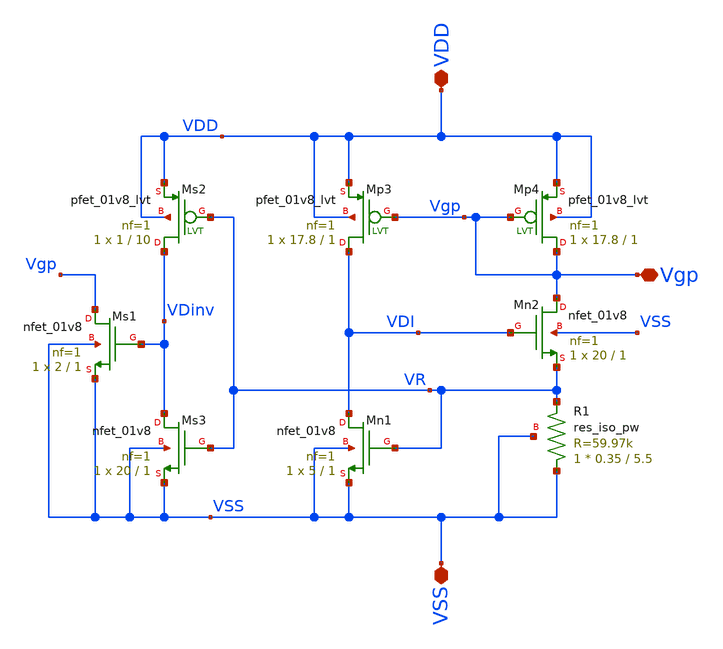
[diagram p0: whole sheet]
** sch_path: xschem/Iref/self_bias.sch
**.subckt self_bias Vgp VDD VSS
*.iopin Vgp
*.iopin VDD
*.iopin VSS
XMn1 VDI VR VSS VSS sky130_fd_pr__nfet_01v8 L=1 W=5 nf=1 ad='int((1 + 1)/2) * 5 / 1 * 0.29' as='int((1 + 2)/2) * 5 / 1 * 0.29'
+ pd='2*int((1 + 1)/2) * (5 / 1 + 0.29)' ps='2*int((1 + 2)/2) * (5 / 1 + 0.29)' nrd='0.29 / 5 ' nrs='0.29 / 5 '
+ sa=0 sb=0 sd=0 mult=1 m=1
XMn2 Vgp VDI VR VSS sky130_fd_pr__nfet_01v8 L=1 W=20 nf=1 ad='int((1 + 1)/2) * 20 / 1 * 0.29' as='int((1 + 2)/2) * 20 / 1 * 0.29'
+ pd='2*int((1 + 1)/2) * (20 / 1 + 0.29)' ps='2*int((1 + 2)/2) * (20 / 1 + 0.29)' nrd='0.29 / 20 ' nrs='0.29 / 20 '
+ sa=0 sb=0 sd=0 mult=1 m=1
XMs3 VDinv VR VSS VSS sky130_fd_pr__nfet_01v8 L=1 W=20 nf=1 ad='int((1 + 1)/2) * 20 / 1 * 0.29' as='int((1 + 2)/2) * 20 / 1 * 0.29'
+ pd='2*int((1 + 1)/2) * (20 / 1 + 0.29)' ps='2*int((1 + 2)/2) * (20 / 1 + 0.29)' nrd='0.29 / 20 ' nrs='0.29 / 20 '
+ sa=0 sb=0 sd=0 mult=1 m=1
XMs1 Vgp VDinv VSS VSS sky130_fd_pr__nfet_01v8 L=1 W=2 nf=1 ad='int((1 + 1)/2) * 2 / 1 * 0.29' as='int((1 + 2)/2) * 2 / 1 * 0.29'
+ pd='2*int((1 + 1)/2) * (2 / 1 + 0.29)' ps='2*int((1 + 2)/2) * (2 / 1 + 0.29)' nrd='0.29 / 2 ' nrs='0.29 / 2 '
+ sa=0 sb=0 sd=0 mult=1 m=1
XMp4 Vgp Vgp VDD VDD sky130_fd_pr__pfet_01v8_lvt L=1 W=17.8 nf=1 ad='int((1 + 1)/2) * 17.8 / 1 * 0.29'
+ as='int((1 + 2)/2) * 17.8 / 1 * 0.29' pd='2*int((1 + 1)/2) * (17.8 / 1 + 0.29)' ps='2*int((1 + 2)/2) * (17.8 / 1 + 0.29)'
+ nrd='0.29 / 17.8 ' nrs='0.29 / 17.8 ' sa=0 sb=0 sd=0 mult=1 m=1
XMp3 VDI Vgp VDD VDD sky130_fd_pr__pfet_01v8_lvt L=1 W=17.8 nf=1 ad='int((1 + 1)/2) * 17.8 / 1 * 0.29'
+ as='int((1 + 2)/2) * 17.8 / 1 * 0.29' pd='2*int((1 + 1)/2) * (17.8 / 1 + 0.29)' ps='2*int((1 + 2)/2) * (17.8 / 1 + 0.29)'
+ nrd='0.29 / 17.8 ' nrs='0.29 / 17.8 ' sa=0 sb=0 sd=0 mult=1 m=1
XMs2 VDinv VR VDD VDD sky130_fd_pr__pfet_01v8_lvt L=10 W=1 nf=1 ad='int((1 + 1)/2) * 1 / 1 * 0.29' as='int((1 + 2)/2) * 1 / 1 * 0.29'
+ pd='2*int((1 + 1)/2) * (1 / 1 + 0.29)' ps='2*int((1 + 2)/2) * (1 / 1 + 0.29)' nrd='0.29 / 1 ' nrs='0.29 / 1 '
+ sa=0 sb=0 sd=0 mult=1 m=1
XR1 VSS VR VSS sky130_fd_pr__res_iso_pw W=0.35 L=5.5 m=1
**.ends
.end
